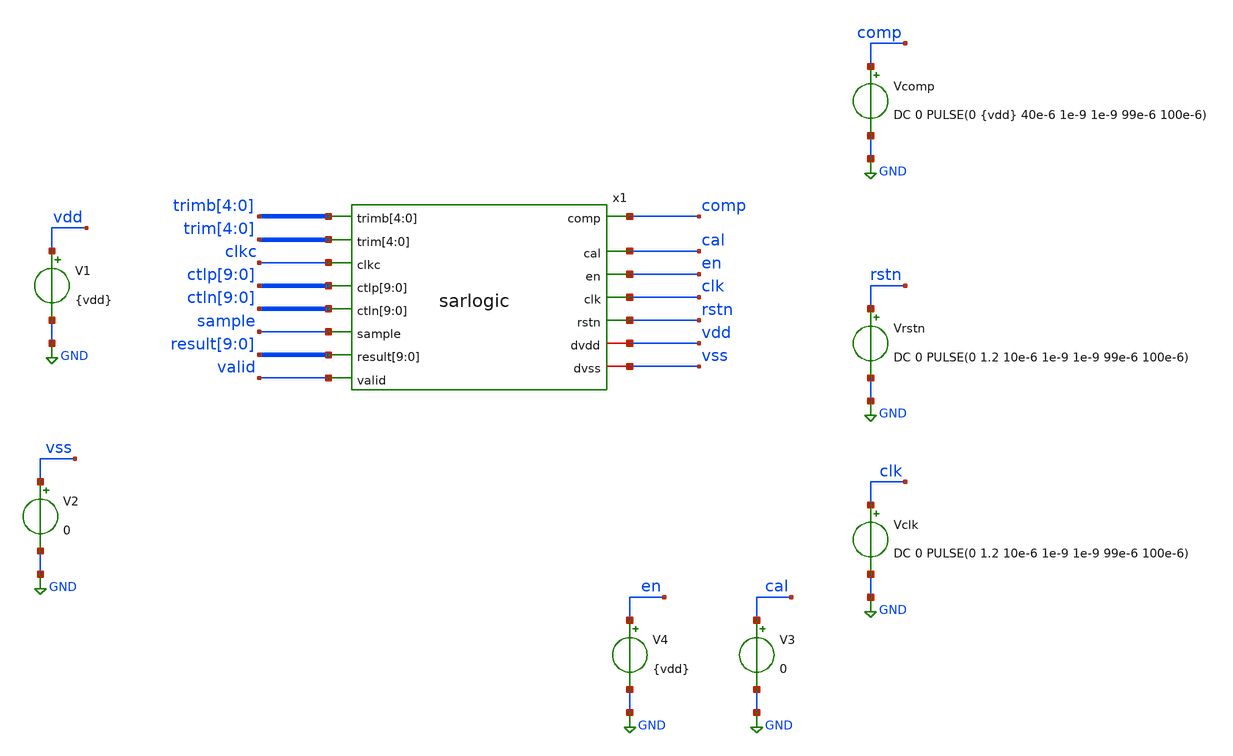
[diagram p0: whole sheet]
** sch_path: xschem/adc/tb_sarlogic.sch
**.subckt tb_sarlogic
x1 vdd vss trimb[4] trimb[3] trimb[2] trimb[1] trimb[0] comp cal trim[4] trim[3] trim[2] trim[1]
+ trim[0] en clk clkc sample result[9] result[8] result[7] result[6] result[5] result[4] result[3] result[2]
+ result[1] result[0] ctlp[9] ctlp[8] ctlp[7] ctlp[6] ctlp[5] ctlp[4] ctlp[3] ctlp[2] ctlp[1] ctlp[0] valid
+ ctln[9] ctln[8] ctln[7] ctln[6] ctln[5] ctln[4] ctln[3] ctln[2] ctln[1] ctln[0] rstn sarlogic
Vcomp comp GND DC 0 PULSE(0 {vdd} 40e-6 1e-9 1e-9 99e-6 100e-6)
Vrstn rstn GND DC 0 PULSE(0 1.2 10e-6 1e-9 1e-9 99e-6 100e-6)
Vclk clk GND DC 0 PULSE(0 1.2 10e-6 1e-9 1e-9 99e-6 100e-6)
V3 cal GND 0
V4 en GND {vdd}
V1 vdd GND {vdd}
V2 vss GND 0
**** begin user architecture code
 *.options method = trap
*.options gmin   = 1e-12
*.options abstol = 1e-8
*.options chtol  = 1e-18
*.options reltol = 0.01
*.options vntol  = 0.1e-6

*.options rshunt = 10e-12

.param MC_SWITCH=0

.ic v(valid)=0
.ic v(sample)=0
.ic v(clkc)=0

.ic v(trim_0_)=0
.ic v(trim_1_)=0
.ic v(trim_2_)=0
.ic v(trim_3_)=0
.ic v(trim_4_)=0
.ic v(trimb_0_)=0
.ic v(trimb_1_)=0
.ic v(trimb_2_)=0
.ic v(trimb_3_)=0
.ic v(trimb_4_)=0


.ic v(result_0_)=0
.ic v(result_1_)=0
.ic v(result_2_)=0
.ic v(result_3_)=0
.ic v(result_4_)=0
.ic v(result_5_)=0
.ic v(result_6_)=0
.ic v(result_7_)=0
.ic v(result_8_)=0
.ic v(result_9_)=0

.ic v(ctlp_0_)=0
.ic v(ctlp_1_)=0
.ic v(ctlp_2_)=0
.ic v(ctlp_3_)=0
.ic v(ctlp_4_)=0
.ic v(ctlp_5_)=0
.ic v(ctlp_6_)=0
.ic v(ctlp_7_)=0
.ic v(ctlp_8_)=0
.ic v(ctlp_9_)=0

.ic v(ctln_0_)=0
.ic v(ctln_1_)=0
.ic v(ctln_2_)=0
.ic v(ctln_3_)=0
.ic v(ctln_4_)=0
.ic v(ctln_5_)=0
.ic v(ctln_6_)=0
.ic v(ctln_7_)=0
.ic v(ctln_8_)=0
.ic v(ctln_9_)=0

.include /home/oe23ranan/caravel_user_project_analog/xschem/adc/sarlogic.ext.spice

.param vdd=1.2

*.tran 100e-9 68e-6
.tran 100e-9 68e-6 uic

.control
run

echo Simulation Finished
echo -------------------
shell date
echo -------------------

.endc

 * FET CORNERS
.include $::SKYWATER_MODELS/corners/tt.spice
*.include $::SKYWATER_MODELS/corners/ff.spice
*.include $::SKYWATER_MODELS/corners/ss.spice
*.include $::SKYWATER_MODELS/corners/sf.spice
*.include $::SKYWATER_MODELS/corners/fs.spice

* TT + R + C
*.include $::SKYWATER_MODELS/corners/tt_rmax_cmax.spice
*.include $::SKYWATER_MODELS/corners/tt_rmin_cmin.spice
*.include $::SKYWATER_MODELS/corners/tt_rmax_cmin.spice
*.include $::SKYWATER_MODELS/corners/tt_rmin_cmax.spice

* FF + R + C
*.include $::SKYWATER_MODELS/corners/ff_rmax_cmax.spice
*.include $::SKYWATER_MODELS/corners/ff_rmin_cmin.spice
*.include $::SKYWATER_MODELS/corners/ff_rmax_cmin.spice
*.include $::SKYWATER_MODELS/corners/ff_rmin_cmax.spice


* SS + R + C
*.include $::SKYWATER_MODELS/corners/ss_rmax_cmax.spice
*.include $::SKYWATER_MODELS/corners/ss_rmin_cmin.spice
*.include $::SKYWATER_MODELS/corners/ss_rmax_cmin.spice
*.include $::SKYWATER_MODELS/corners/ss_rmin_cmax.spice

* SF + R + C
*.include $::SKYWATER_MODELS/corners/sf_rmax_cmax.spice
*.include $::SKYWATER_MODELS/corners/sf_rmin_cmin.spice
*.include $::SKYWATER_MODELS/corners/sf_rmax_cmin.spice
*.include $::SKYWATER_MODELS/corners/sf_rmin_cmax.spice

* FS + R + C
*.include $::SKYWATER_MODELS/corners/fs_rmax_cmax.spice
*.include $::SKYWATER_MODELS/corners/fs_rmin_cmin.spice
*.include $::SKYWATER_MODELS/corners/fs_rmax_cmin.spice
*.include $::SKYWATER_MODELS/corners/fs_rmin_cmax.spice

.include $::SKYWATER_STDCELLS/cells/inv/sky130_fd_sc_hd__inv_4.spice
.include $::SKYWATER_STDCELLS/cells/decap/sky130_fd_sc_hd__decap_8.spice
.include $::SKYWATER_STDCELLS/cells/decap/sky130_fd_sc_hd__decap_3.spice
.include $::SKYWATER_STDCELLS/cells/buf/sky130_fd_sc_hd__buf_1.spice
.include $::SKYWATER_STDCELLS/cells/inv/sky130_fd_sc_hd__inv_1.spice
.include $::SKYWATER_STDCELLS/cells/inv/sky130_fd_sc_hd__inv_2.spice
.include $::SKYWATER_STDCELLS/cells/tap/sky130_fd_sc_hd__tap_2.spice
**** end user architecture code
**.ends

* expanding   symbol:  adc/sarlogic.sym # of pins=15
** sym_path: xschem/adc/sarlogic.sym
** sch_path: xschem/adc/sarlogic.sch
.subckt sarlogic dvdd dvss trimb[4] trimb[3] trimb[2] trimb[1] trimb[0] comp cal trim[4] trim[3]
+ trim[2] trim[1] trim[0] en clk clkc sample result[9] result[8] result[7] result[6] result[5] result[4]
+ result[3] result[2] result[1] result[0] ctlp[9] ctlp[8] ctlp[7] ctlp[6] ctlp[5] ctlp[4] ctlp[3] ctlp[2]
+ ctlp[1] ctlp[0] valid ctln[9] ctln[8] ctln[7] ctln[6] ctln[5] ctln[4] ctln[3] ctln[2] ctln[1] ctln[0] rstn
*.ipin comp
*.ipin cal
*.ipin en
*.ipin clk
*.ipin valid
*.ipin rstn
*.ipin
*+ result[9],result[8],result[7],result[6],result[5],result[4],result[3],result[2],result[1],result[0]
*.opin trimb[4],trimb[3],trimb[2],trimb[1],trimb[0]
*.opin trim[4],trim[3],trim[2],trim[1],trim[0]
*.opin clkc
*.opin sample
*.opin ctlp[9],ctlp[8],ctlp[7],ctlp[6],ctlp[5],ctlp[4],ctlp[3],ctlp[2],ctlp[1],ctlp[0]
*.opin ctln[9],ctln[8],ctln[7],ctln[6],ctln[5],ctln[4],ctln[3],ctln[2],ctln[1],ctln[0]
*.iopin dvdd
*.iopin dvss
* noconn comp
* noconn rstn
* noconn valid
* noconn cal
* noconn en
* noconn clk
* noconn result[9:0]
* noconn trimb[4:0]
* noconn ctln[9:0]
* noconn trim[4:0]
* noconn ctlp[9:0]
* noconn sample
* noconn clkc
* noconn dvdd
* noconn dvss
**** begin user architecture code
.include /home/oe23ranan/caravel_user_project_analog/xschem/adc/cmos_cells_digital.sp
.include /home/oe23ranan/caravel_user_project_analog/xschem/adc/sarlogic.sp

**** end user architecture code
.ends

.GLOBAL GND
.end
